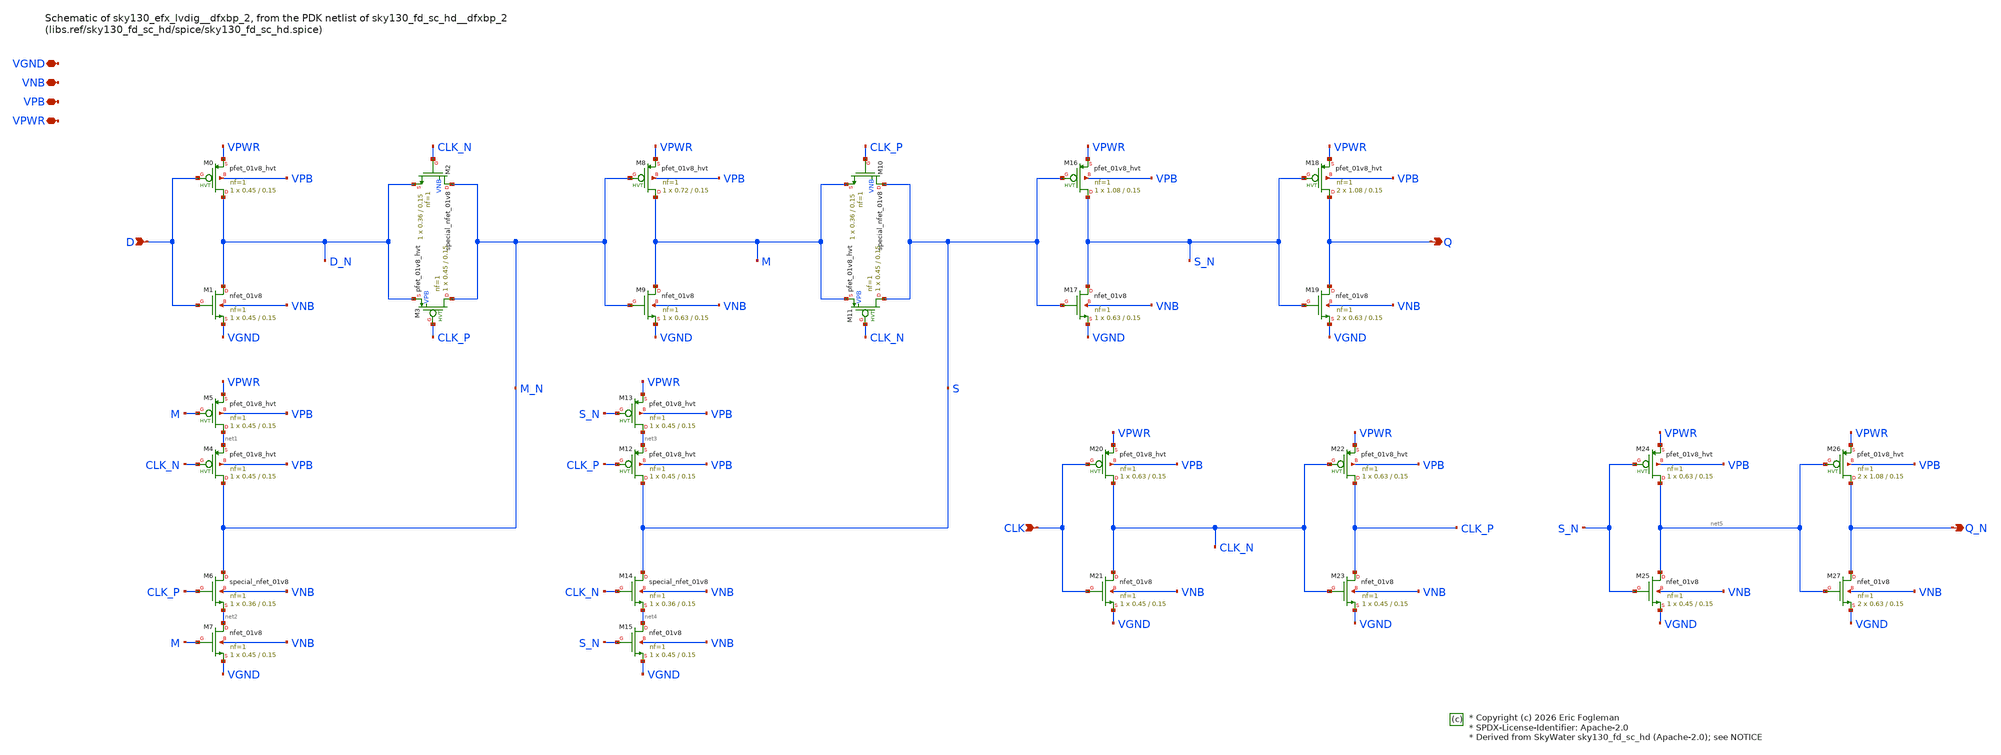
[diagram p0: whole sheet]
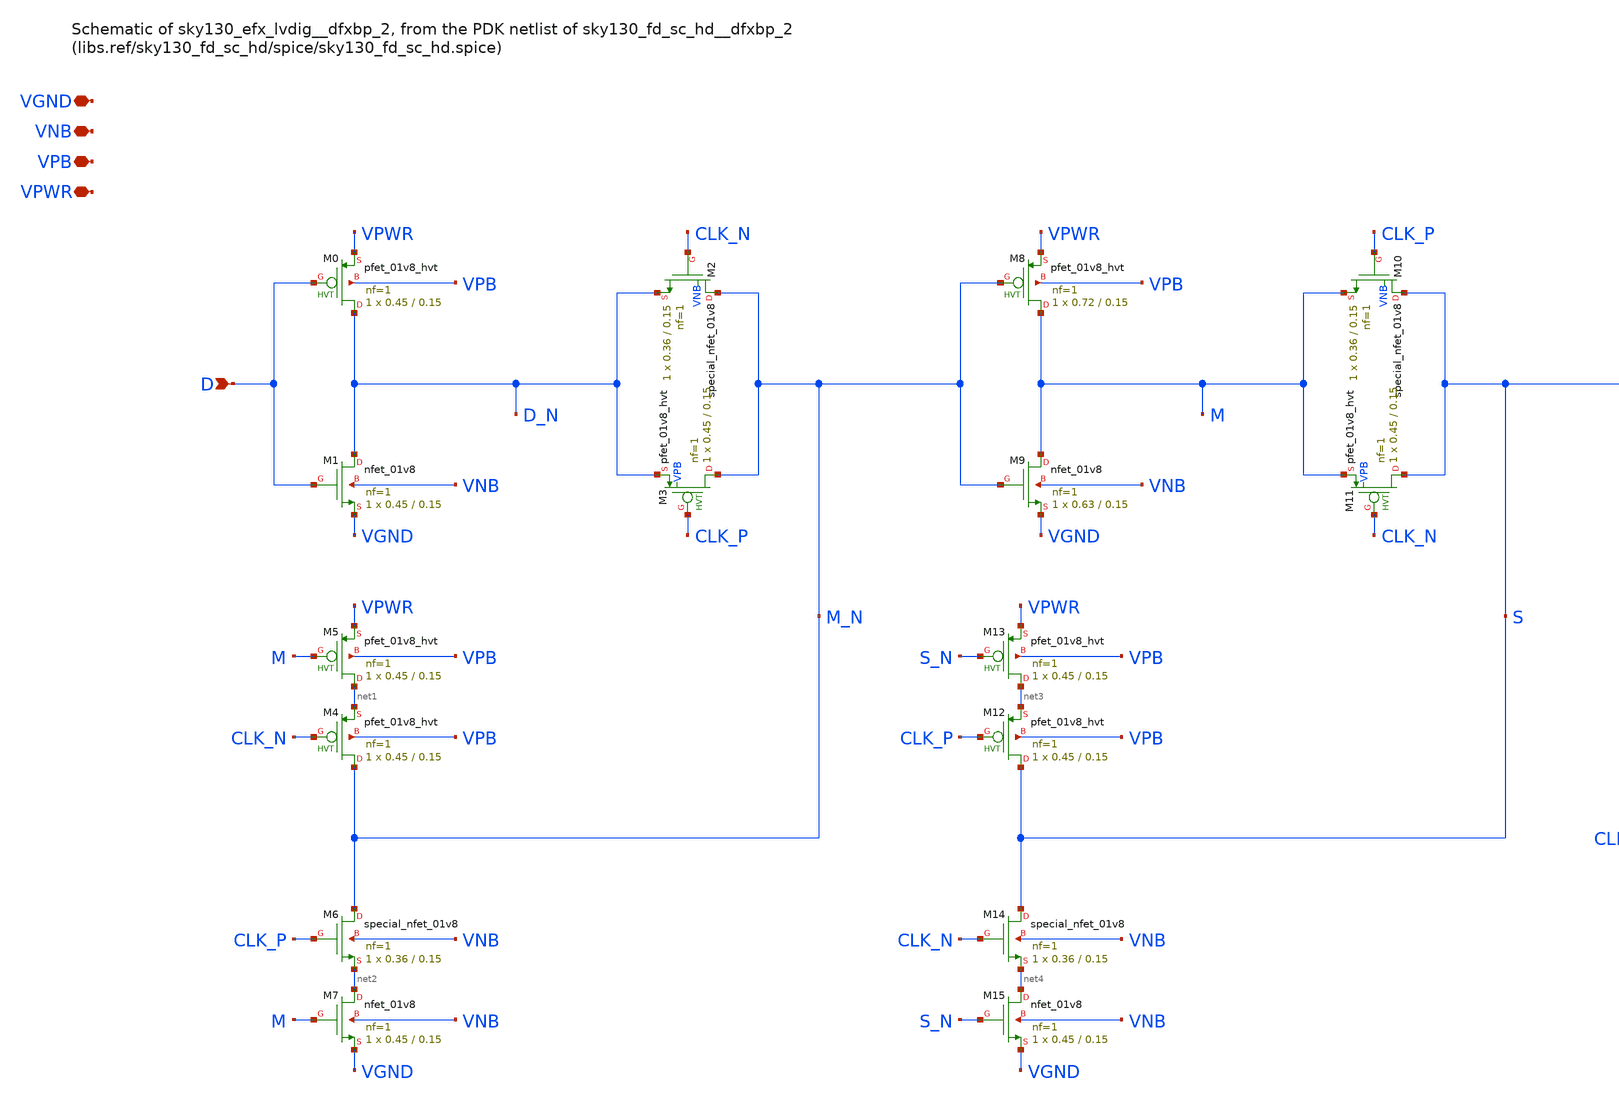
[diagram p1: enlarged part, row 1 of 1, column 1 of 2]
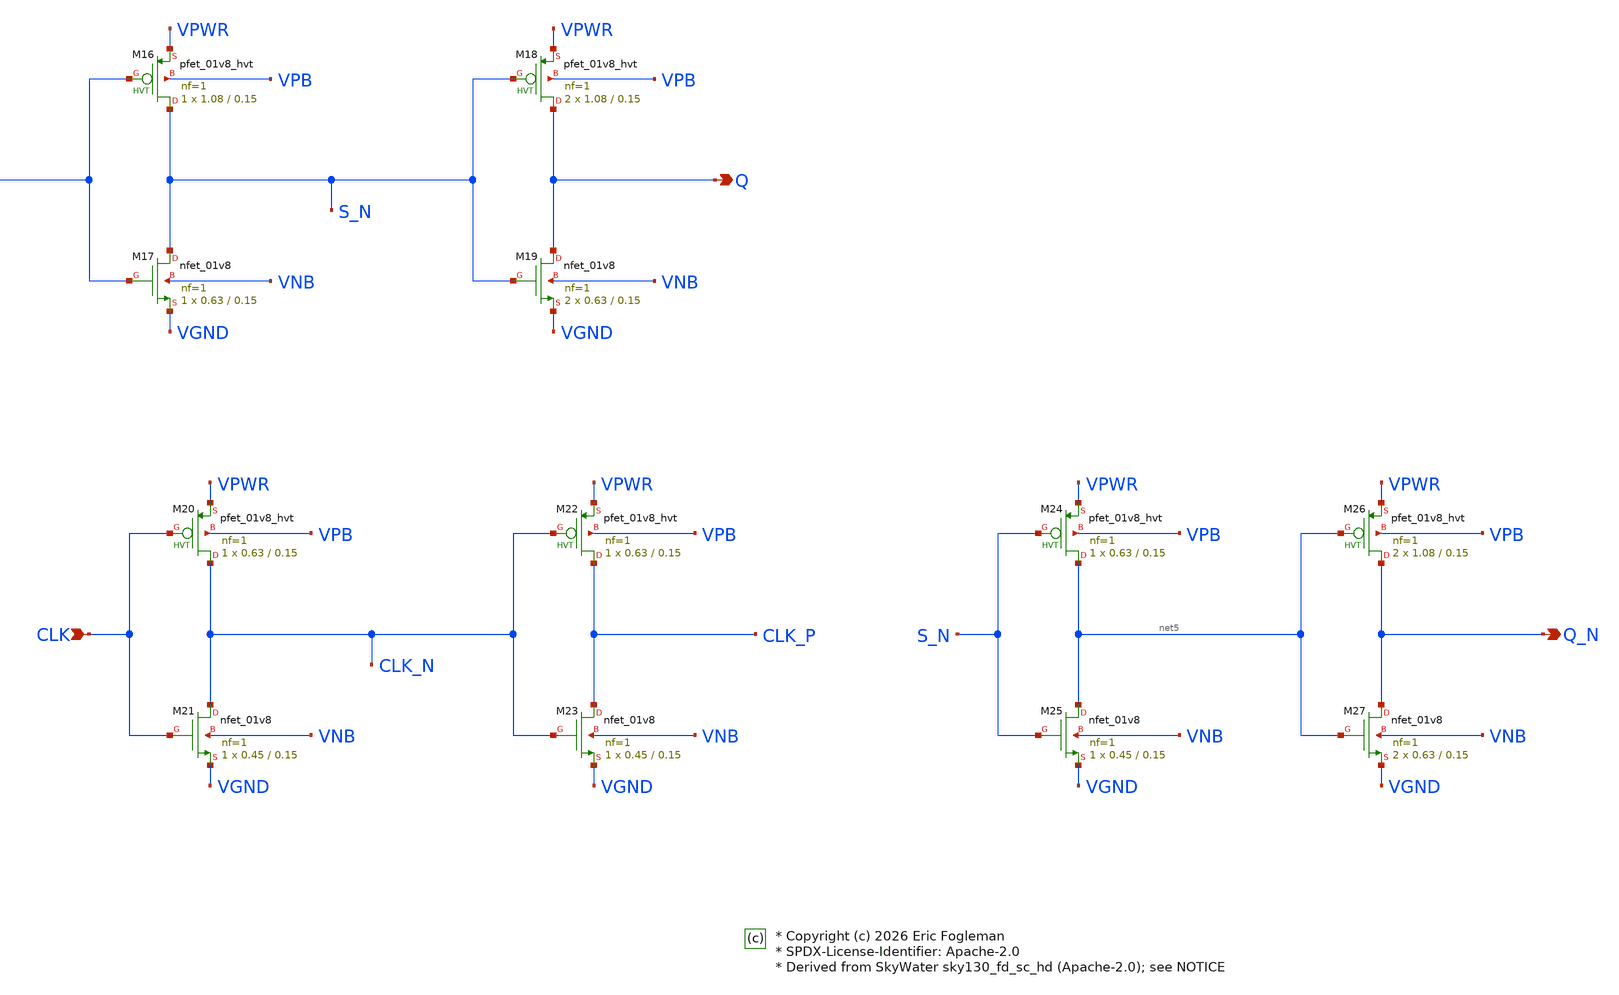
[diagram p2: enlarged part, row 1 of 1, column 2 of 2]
** sch_path: xschem/sky130_efx_lvdig__dfxbp_2.sch

* Copyright (c) 2026 Eric Fogleman
* SPDX-License-Identifier: Apache-2.0
* Derived from SkyWater sky130_fd_sc_hd (Apache-2.0); see NOTICE

**.subckt sky130_efx_lvdig__dfxbp_2 D Q CLK Q_N VGND VNB VPB VPWR
*.ipin D
*.opin Q
*.ipin CLK
*.opin Q_N
*.iopin VGND
*.iopin VNB
*.iopin VPB
*.iopin VPWR
XM0 D_N D VPWR VPB sky130_fd_pr__pfet_01v8_hvt L=0.15 W=0.45 nf=1 ad='int((1 + 1)/2) * 0.45 / 1 * 0.29'
+ as='int((1 + 2)/2) * 0.45 / 1 * 0.29' pd='2*int((1 + 1)/2) * (0.45 / 1 + 0.29)' ps='2*int((1 + 2)/2) * (0.45 / 1 + 0.29)'
+ nrd='0.29 / 0.45 ' nrs='0.29 / 0.45 ' sa=0 sb=0 sd=0 mult=1 m=1
XM1 D_N D VGND VNB sky130_fd_pr__nfet_01v8 L=0.15 W=0.45 nf=1 ad='int((1 + 1)/2) * 0.45 / 1 * 0.29' as='int((1 + 2)/2) * 0.45 / 1 * 0.29'
+ pd='2*int((1 + 1)/2) * (0.45 / 1 + 0.29)' ps='2*int((1 + 2)/2) * (0.45 / 1 + 0.29)' nrd='0.29 / 0.45 '
+ nrs='0.29 / 0.45 ' sa=0 sb=0 sd=0 mult=1 m=1
XM2 M_N CLK_N D_N VNB sky130_fd_pr__special_nfet_01v8 L=0.15 W=0.36 nf=1 ad='int((nf+1)/2) * W/nf * 0.29'
+ as='int((nf+2)/2) * W/nf * 0.29' pd='2*int((nf+1)/2) * (W/nf + 0.29)' ps='2*int((nf+2)/2) * (W/nf + 0.29)'
+ nrd='0.29 / W' nrs='0.29 / W' sa=0 sb=0 sd=0 mult=1 m=1
XM3 M_N CLK_P D_N VPB sky130_fd_pr__pfet_01v8_hvt L=0.15 W=0.45 nf=1 ad='int((1 + 1)/2) * 0.45 / 1 * 0.29'
+ as='int((1 + 2)/2) * 0.45 / 1 * 0.29' pd='2*int((1 + 1)/2) * (0.45 / 1 + 0.29)' ps='2*int((1 + 2)/2) * (0.45 / 1 + 0.29)'
+ nrd='0.29 / 0.45 ' nrs='0.29 / 0.45 ' sa=0 sb=0 sd=0 mult=1 m=1
XM4 M_N CLK_N net1 VPB sky130_fd_pr__pfet_01v8_hvt L=0.15 W=0.45 nf=1 ad='int((1 + 1)/2) * 0.45 / 1 * 0.29'
+ as='int((1 + 2)/2) * 0.45 / 1 * 0.29' pd='2*int((1 + 1)/2) * (0.45 / 1 + 0.29)' ps='2*int((1 + 2)/2) * (0.45 / 1 + 0.29)'
+ nrd='0.29 / 0.45 ' nrs='0.29 / 0.45 ' sa=0 sb=0 sd=0 mult=1 m=1
XM5 net1 M VPWR VPB sky130_fd_pr__pfet_01v8_hvt L=0.15 W=0.45 nf=1 ad='int((1 + 1)/2) * 0.45 / 1 * 0.29'
+ as='int((1 + 2)/2) * 0.45 / 1 * 0.29' pd='2*int((1 + 1)/2) * (0.45 / 1 + 0.29)' ps='2*int((1 + 2)/2) * (0.45 / 1 + 0.29)'
+ nrd='0.29 / 0.45 ' nrs='0.29 / 0.45 ' sa=0 sb=0 sd=0 mult=1 m=1
XM6 M_N CLK_P net2 VNB sky130_fd_pr__special_nfet_01v8 L=0.15 W=0.36 nf=1 ad='int((1 + 1)/2) * 0.36 / 1 * 0.29'
+ as='int((1 + 2)/2) * 0.36 / 1 * 0.29' pd='2*int((1 + 1)/2) * (0.36 / 1 + 0.29)' ps='2*int((1 + 2)/2) * (0.36 / 1 + 0.29)'
+ nrd='0.29 / 0.36 ' nrs='0.29 / 0.36 ' sa=0 sb=0 sd=0 mult=1 m=1
XM7 net2 M VGND VNB sky130_fd_pr__nfet_01v8 L=0.15 W=0.45 nf=1 ad='int((1 + 1)/2) * 0.45 / 1 * 0.29'
+ as='int((1 + 2)/2) * 0.45 / 1 * 0.29' pd='2*int((1 + 1)/2) * (0.45 / 1 + 0.29)' ps='2*int((1 + 2)/2) * (0.45 / 1 + 0.29)'
+ nrd='0.29 / 0.45 ' nrs='0.29 / 0.45 ' sa=0 sb=0 sd=0 mult=1 m=1
XM8 M M_N VPWR VPB sky130_fd_pr__pfet_01v8_hvt L=0.15 W=0.72 nf=1 ad='int((1 + 1)/2) * 0.72 / 1 * 0.29'
+ as='int((1 + 2)/2) * 0.72 / 1 * 0.29' pd='2*int((1 + 1)/2) * (0.72 / 1 + 0.29)' ps='2*int((1 + 2)/2) * (0.72 / 1 + 0.29)'
+ nrd='0.29 / 0.72 ' nrs='0.29 / 0.72 ' sa=0 sb=0 sd=0 mult=1 m=1
XM9 M M_N VGND VNB sky130_fd_pr__nfet_01v8 L=0.15 W=0.63 nf=1 ad='int((1 + 1)/2) * 0.63 / 1 * 0.29' as='int((1 + 2)/2) * 0.63 / 1 * 0.29'
+ pd='2*int((1 + 1)/2) * (0.63 / 1 + 0.29)' ps='2*int((1 + 2)/2) * (0.63 / 1 + 0.29)' nrd='0.29 / 0.63 '
+ nrs='0.29 / 0.63 ' sa=0 sb=0 sd=0 mult=1 m=1
XM10 S CLK_P M VNB sky130_fd_pr__special_nfet_01v8 L=0.15 W=0.36 nf=1 ad='int((nf+1)/2) * W/nf * 0.29'
+ as='int((nf+2)/2) * W/nf * 0.29' pd='2*int((nf+1)/2) * (W/nf + 0.29)' ps='2*int((nf+2)/2) * (W/nf + 0.29)'
+ nrd='0.29 / W' nrs='0.29 / W' sa=0 sb=0 sd=0 mult=1 m=1
XM11 S CLK_N M VPB sky130_fd_pr__pfet_01v8_hvt L=0.15 W=0.45 nf=1 ad='int((1 + 1)/2) * 0.45 / 1 * 0.29'
+ as='int((1 + 2)/2) * 0.45 / 1 * 0.29' pd='2*int((1 + 1)/2) * (0.45 / 1 + 0.29)' ps='2*int((1 + 2)/2) * (0.45 / 1 + 0.29)'
+ nrd='0.29 / 0.45 ' nrs='0.29 / 0.45 ' sa=0 sb=0 sd=0 mult=1 m=1
XM12 S CLK_P net3 VPB sky130_fd_pr__pfet_01v8_hvt L=0.15 W=0.45 nf=1 ad='int((1 + 1)/2) * 0.45 / 1 * 0.29'
+ as='int((1 + 2)/2) * 0.45 / 1 * 0.29' pd='2*int((1 + 1)/2) * (0.45 / 1 + 0.29)' ps='2*int((1 + 2)/2) * (0.45 / 1 + 0.29)'
+ nrd='0.29 / 0.45 ' nrs='0.29 / 0.45 ' sa=0 sb=0 sd=0 mult=1 m=1
XM13 net3 S_N VPWR VPB sky130_fd_pr__pfet_01v8_hvt L=0.15 W=0.45 nf=1 ad='int((1 + 1)/2) * 0.45 / 1 * 0.29'
+ as='int((1 + 2)/2) * 0.45 / 1 * 0.29' pd='2*int((1 + 1)/2) * (0.45 / 1 + 0.29)' ps='2*int((1 + 2)/2) * (0.45 / 1 + 0.29)'
+ nrd='0.29 / 0.45 ' nrs='0.29 / 0.45 ' sa=0 sb=0 sd=0 mult=1 m=1
XM14 S CLK_N net4 VNB sky130_fd_pr__special_nfet_01v8 L=0.15 W=0.36 nf=1 ad='int((1 + 1)/2) * 0.36 / 1 * 0.29'
+ as='int((1 + 2)/2) * 0.36 / 1 * 0.29' pd='2*int((1 + 1)/2) * (0.36 / 1 + 0.29)' ps='2*int((1 + 2)/2) * (0.36 / 1 + 0.29)'
+ nrd='0.29 / 0.36 ' nrs='0.29 / 0.36 ' sa=0 sb=0 sd=0 mult=1 m=1
XM15 net4 S_N VGND VNB sky130_fd_pr__nfet_01v8 L=0.15 W=0.45 nf=1 ad='int((1 + 1)/2) * 0.45 / 1 * 0.29'
+ as='int((1 + 2)/2) * 0.45 / 1 * 0.29' pd='2*int((1 + 1)/2) * (0.45 / 1 + 0.29)' ps='2*int((1 + 2)/2) * (0.45 / 1 + 0.29)'
+ nrd='0.29 / 0.45 ' nrs='0.29 / 0.45 ' sa=0 sb=0 sd=0 mult=1 m=1
XM16 S_N S VPWR VPB sky130_fd_pr__pfet_01v8_hvt L=0.15 W=1.08 nf=1 ad='int((1 + 1)/2) * 1.08 / 1 * 0.29'
+ as='int((1 + 2)/2) * 1.08 / 1 * 0.29' pd='2*int((1 + 1)/2) * (1.08 / 1 + 0.29)' ps='2*int((1 + 2)/2) * (1.08 / 1 + 0.29)'
+ nrd='0.29 / 1.08 ' nrs='0.29 / 1.08 ' sa=0 sb=0 sd=0 mult=1 m=1
XM17 S_N S VGND VNB sky130_fd_pr__nfet_01v8 L=0.15 W=0.63 nf=1 ad='int((1 + 1)/2) * 0.63 / 1 * 0.29'
+ as='int((1 + 2)/2) * 0.63 / 1 * 0.29' pd='2*int((1 + 1)/2) * (0.63 / 1 + 0.29)' ps='2*int((1 + 2)/2) * (0.63 / 1 + 0.29)'
+ nrd='0.29 / 0.63 ' nrs='0.29 / 0.63 ' sa=0 sb=0 sd=0 mult=1 m=1
XM18 Q S_N VPWR VPB sky130_fd_pr__pfet_01v8_hvt L=0.15 W=1.08 nf=1 ad='int((1 + 1)/2) * 1.08 / 1 * 0.29'
+ as='int((1 + 2)/2) * 1.08 / 1 * 0.29' pd='2*int((1 + 1)/2) * (1.08 / 1 + 0.29)' ps='2*int((1 + 2)/2) * (1.08 / 1 + 0.29)'
+ nrd='0.29 / 1.08 ' nrs='0.29 / 1.08 ' sa=0 sb=0 sd=0 mult=2 m=2
XM19 Q S_N VGND VNB sky130_fd_pr__nfet_01v8 L=0.15 W=0.63 nf=1 ad='int((1 + 1)/2) * 0.63 / 1 * 0.29'
+ as='int((1 + 2)/2) * 0.63 / 1 * 0.29' pd='2*int((1 + 1)/2) * (0.63 / 1 + 0.29)' ps='2*int((1 + 2)/2) * (0.63 / 1 + 0.29)'
+ nrd='0.29 / 0.63 ' nrs='0.29 / 0.63 ' sa=0 sb=0 sd=0 mult=2 m=2
XM20 CLK_N CLK VPWR VPB sky130_fd_pr__pfet_01v8_hvt L=0.15 W=0.63 nf=1 ad='int((1 + 1)/2) * 0.63 / 1 * 0.29'
+ as='int((1 + 2)/2) * 0.63 / 1 * 0.29' pd='2*int((1 + 1)/2) * (0.63 / 1 + 0.29)' ps='2*int((1 + 2)/2) * (0.63 / 1 + 0.29)'
+ nrd='0.29 / 0.63 ' nrs='0.29 / 0.63 ' sa=0 sb=0 sd=0 mult=1 m=1
XM21 CLK_N CLK VGND VNB sky130_fd_pr__nfet_01v8 L=0.15 W=0.45 nf=1 ad='int((1 + 1)/2) * 0.45 / 1 * 0.29'
+ as='int((1 + 2)/2) * 0.45 / 1 * 0.29' pd='2*int((1 + 1)/2) * (0.45 / 1 + 0.29)' ps='2*int((1 + 2)/2) * (0.45 / 1 + 0.29)'
+ nrd='0.29 / 0.45 ' nrs='0.29 / 0.45 ' sa=0 sb=0 sd=0 mult=1 m=1
XM22 CLK_P CLK_N VPWR VPB sky130_fd_pr__pfet_01v8_hvt L=0.15 W=0.63 nf=1 ad='int((1 + 1)/2) * 0.63 / 1 * 0.29'
+ as='int((1 + 2)/2) * 0.63 / 1 * 0.29' pd='2*int((1 + 1)/2) * (0.63 / 1 + 0.29)' ps='2*int((1 + 2)/2) * (0.63 / 1 + 0.29)'
+ nrd='0.29 / 0.63 ' nrs='0.29 / 0.63 ' sa=0 sb=0 sd=0 mult=1 m=1
XM23 CLK_P CLK_N VGND VNB sky130_fd_pr__nfet_01v8 L=0.15 W=0.45 nf=1 ad='int((1 + 1)/2) * 0.45 / 1 * 0.29'
+ as='int((1 + 2)/2) * 0.45 / 1 * 0.29' pd='2*int((1 + 1)/2) * (0.45 / 1 + 0.29)' ps='2*int((1 + 2)/2) * (0.45 / 1 + 0.29)'
+ nrd='0.29 / 0.45 ' nrs='0.29 / 0.45 ' sa=0 sb=0 sd=0 mult=1 m=1
XM24 net5 S_N VPWR VPB sky130_fd_pr__pfet_01v8_hvt L=0.15 W=0.63 nf=1 ad='int((1 + 1)/2) * 0.63 / 1 * 0.29'
+ as='int((1 + 2)/2) * 0.63 / 1 * 0.29' pd='2*int((1 + 1)/2) * (0.63 / 1 + 0.29)' ps='2*int((1 + 2)/2) * (0.63 / 1 + 0.29)'
+ nrd='0.29 / 0.63 ' nrs='0.29 / 0.63 ' sa=0 sb=0 sd=0 mult=1 m=1
XM25 net5 S_N VGND VNB sky130_fd_pr__nfet_01v8 L=0.15 W=0.45 nf=1 ad='int((1 + 1)/2) * 0.45 / 1 * 0.29'
+ as='int((1 + 2)/2) * 0.45 / 1 * 0.29' pd='2*int((1 + 1)/2) * (0.45 / 1 + 0.29)' ps='2*int((1 + 2)/2) * (0.45 / 1 + 0.29)'
+ nrd='0.29 / 0.45 ' nrs='0.29 / 0.45 ' sa=0 sb=0 sd=0 mult=1 m=1
XM26 Q_N net5 VPWR VPB sky130_fd_pr__pfet_01v8_hvt L=0.15 W=1.08 nf=1 ad='int((1 + 1)/2) * 1.08 / 1 * 0.29'
+ as='int((1 + 2)/2) * 1.08 / 1 * 0.29' pd='2*int((1 + 1)/2) * (1.08 / 1 + 0.29)' ps='2*int((1 + 2)/2) * (1.08 / 1 + 0.29)'
+ nrd='0.29 / 1.08 ' nrs='0.29 / 1.08 ' sa=0 sb=0 sd=0 mult=2 m=2
XM27 Q_N net5 VGND VNB sky130_fd_pr__nfet_01v8 L=0.15 W=0.63 nf=1 ad='int((1 + 1)/2) * 0.63 / 1 * 0.29'
+ as='int((1 + 2)/2) * 0.63 / 1 * 0.29' pd='2*int((1 + 1)/2) * (0.63 / 1 + 0.29)' ps='2*int((1 + 2)/2) * (0.63 / 1 + 0.29)'
+ nrd='0.29 / 0.63 ' nrs='0.29 / 0.63 ' sa=0 sb=0 sd=0 mult=2 m=2
**.ends
.end
